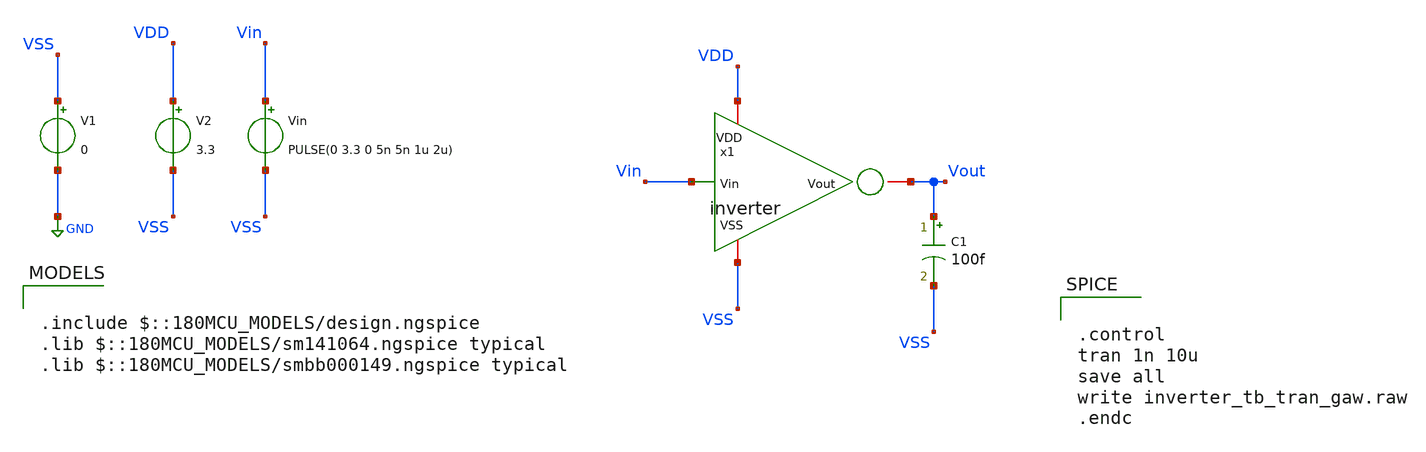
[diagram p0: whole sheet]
** sch_path: gf180_examples/inverter/xschem/inverter_tb_tran_gaw.sch
**.subckt inverter_tb_tran_gaw
x1 Vin VDD VSS Vout inverter
C1 Vout VSS 100f m=1
V1 VSS GND 0
V2 VDD VSS 3.3
Vin Vin VSS PULSE(0 3.3 0 5n 5n 1u 2u)
**** begin user architecture code

.include $::180MCU_MODELS/design.ngspice
.lib $::180MCU_MODELS/sm141064.ngspice typical
.lib $::180MCU_MODELS/smbb000149.ngspice typical



.control
tran 1n 10u
save all
write inverter_tb_tran_gaw.raw
.endc


**** end user architecture code
**.ends
.GLOBAL GND
.end
